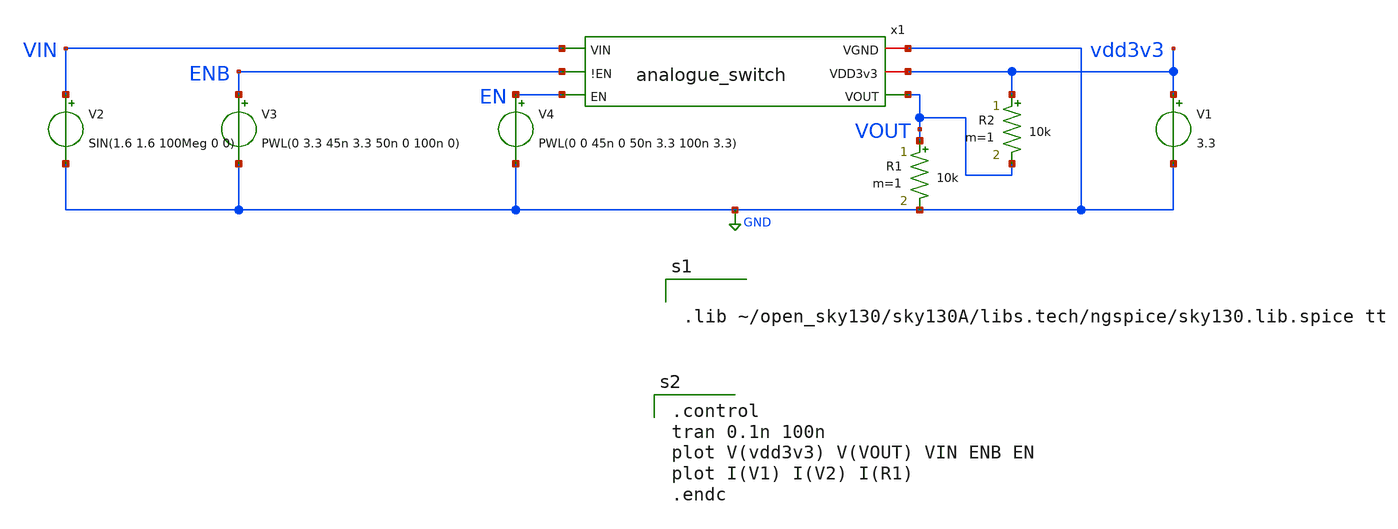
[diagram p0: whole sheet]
** sch_path: xschem/analogue_switch_tb.sch
**.subckt analogue_switch_tb
x1 VIN GND vdd3v3 ENB EN VOUT analogue_switch
V1 vdd3v3 GND 3.3
V2 VIN GND SIN(1.6 1.6 100Meg 0 0)
V3 ENB GND PWL(0 3.3 45n 3.3 50n 0 100n 0)
V4 EN GND PWL(0 0 45n 0 50n 3.3 100n 3.3)
R1 VOUT GND 10k m=1
R2 vdd3v3 VOUT 10k m=1
**** begin user architecture code


.lib ~/open_sky130/sky130A/libs.tech/ngspice/sky130.lib.spice tt


.control
tran 0.1n 100n
plot V(vdd3v3) V(VOUT) VIN ENB EN
plot I(V1) I(V2) I(R1)
.endc

**** end user architecture code
**.ends

* expanding   symbol:  analogue_switch.sym # of pins=6
** sym_path: xschem/analogue_switch.sym
** sch_path: xschem/analogue_switch.sch
.subckt analogue_switch VIN VGND VDD3v3 !EN EN VOUT
*.iopin VGND
*.iopin VDD3v3
*.ipin EN
*.ipin VIN
*.ipin !EN
*.opin VOUT
XM2 VOUT !EN VIN VDD3v3 sky130_fd_pr__pfet_g5v0d10v5 L=0.5 W=1 nf=1 ad='int((nf+1)/2) * W/nf * 0.29'
+ as='int((nf+2)/2) * W/nf * 0.29' pd='2*int((nf+1)/2) * (W/nf + 0.29)' ps='2*int((nf+2)/2) * (W/nf + 0.29)'
+ nrd='0.29 / W' nrs='0.29 / W' sa=0 sb=0 sd=0 mult=15 m=15
XM1 VIN EN VOUT VGND sky130_fd_pr__nfet_03v3_nvt L=0.5 W=1 nf=1 ad='int((nf+1)/2) * W/nf * 0.29' as='int((nf+2)/2) * W/nf * 0.29'
+ pd='2*int((nf+1)/2) * (W/nf + 0.29)' ps='2*int((nf+2)/2) * (W/nf + 0.29)' nrd='0.29 / W' nrs='0.29 / W'
+ sa=0 sb=0 sd=0 mult=10 m=10
.ends

.GLOBAL GND
.end
